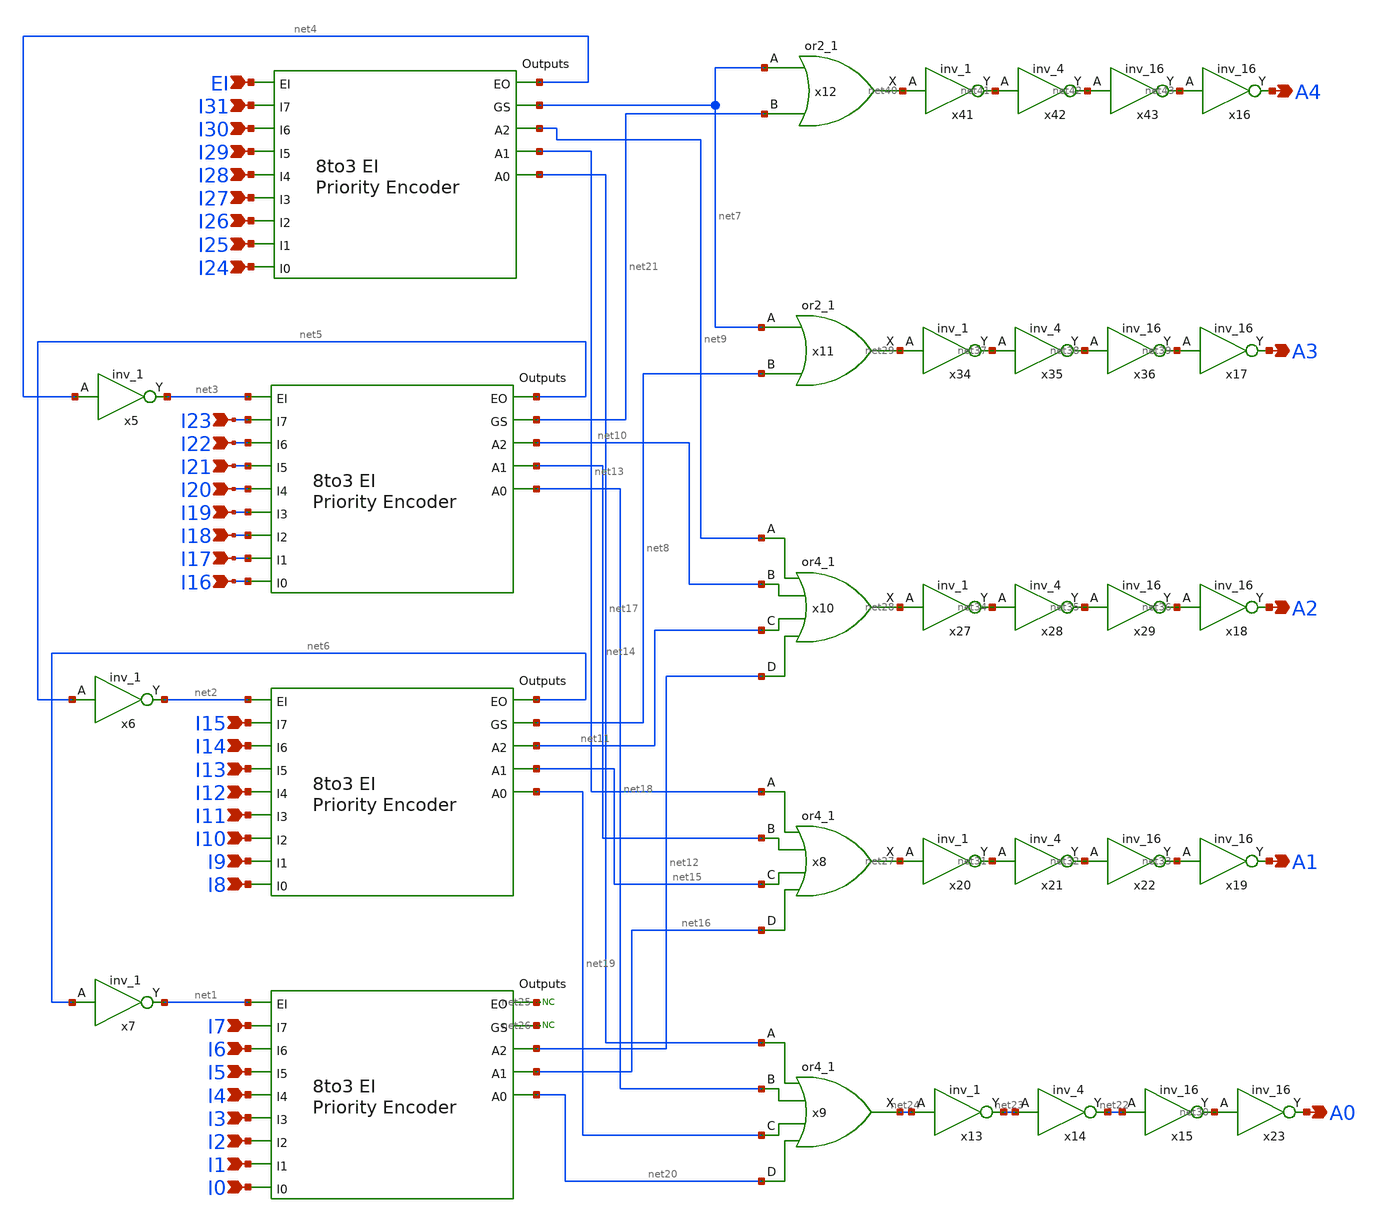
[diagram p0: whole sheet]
** sch_path: PriorityEncoder/32to5_Priority_Encoder_v0p2p2.sch
.lib $::SKYWATER_MODELS/sky130.lib.spice tt
.include $::SKYWATER_STDCELLS/sky130_fd_sc_hd.spice

**.subckt 32to5_Priority_Encoder_v0p2p2 EI I31 I30 I29 I28 I27 I26 I25 I24 I23 I22 I21 I20 I19 I18
*+ I17 I16 I15 I14 I13 I12 I11 I10 I9 I8 I7 I6 I5 I4 I3 I2 I1 I0 A4 A3 A2 A1 A0
*.ipin EI
*.ipin I31
*.ipin I30
*.ipin I29
*.ipin I28
*.ipin I27
*.ipin I26
*.ipin I25
*.ipin I24
*.ipin I23
*.ipin I22
*.ipin I21
*.ipin I20
*.ipin I19
*.ipin I18
*.ipin I17
*.ipin I16
*.ipin I15
*.ipin I14
*.ipin I13
*.ipin I12
*.ipin I11
*.ipin I10
*.ipin I9
*.ipin I8
*.ipin I7
*.ipin I6
*.ipin I5
*.ipin I4
*.ipin I3
*.ipin I2
*.ipin I1
*.ipin I0
*.opin A4
*.opin A3
*.opin A2
*.opin A1
*.opin A0
x1 I25 I29 I27 I24 I26 I30 I31 I28 net4 net7 net9 net13 net17 EI 8to3_Priority_Encoder_v0p2p0
x2 I17 I21 I19 I16 I18 I22 I23 I20 net5 net21 net10 net14 net18 net3 8to3_Priority_Encoder_v0p2p0
x3 I9 I13 I11 I8 I10 I14 I15 I12 net6 net8 net11 net15 net19 net2 8to3_Priority_Encoder_v0p2p0
x4 I1 I5 I3 I0 I2 I6 I7 I4 net25 net26 net12 net16 net20 net1 8to3_Priority_Encoder_v0p2p0
x5 net4 GND GND VDD VDD net3 sky130_fd_sc_hd__inv_1
x9 net17 net18 net19 net20 GND GND VDD VDD net24 sky130_fd_sc_hd__or4_1
x8 net13 net14 net15 net16 GND GND VDD VDD net27 sky130_fd_sc_hd__or4_1
x10 net9 net10 net11 net12 GND GND VDD VDD net28 sky130_fd_sc_hd__or4_1
x11 net7 net8 GND GND VDD VDD net29 sky130_fd_sc_hd__or2_1
x13 net24 GND GND VDD VDD net23 sky130_fd_sc_hd__inv_1
x14 net23 GND GND VDD VDD net22 sky130_fd_sc_hd__inv_4
x15 net22 GND GND VDD VDD net30 sky130_fd_sc_hd__inv_16
x20 net27 GND GND VDD VDD net31 sky130_fd_sc_hd__inv_1
x21 net31 GND GND VDD VDD net32 sky130_fd_sc_hd__inv_4
x22 net32 GND GND VDD VDD net33 sky130_fd_sc_hd__inv_16
x27 net28 GND GND VDD VDD net34 sky130_fd_sc_hd__inv_1
x28 net34 GND GND VDD VDD net35 sky130_fd_sc_hd__inv_4
x29 net35 GND GND VDD VDD net36 sky130_fd_sc_hd__inv_16
x34 net29 GND GND VDD VDD net37 sky130_fd_sc_hd__inv_1
x35 net37 GND GND VDD VDD net38 sky130_fd_sc_hd__inv_4
x36 net38 GND GND VDD VDD net39 sky130_fd_sc_hd__inv_16
x12 net7 net21 GND GND VDD VDD net40 sky130_fd_sc_hd__or2_1
x41 net40 GND GND VDD VDD net41 sky130_fd_sc_hd__inv_1
x42 net41 GND GND VDD VDD net42 sky130_fd_sc_hd__inv_4
x43 net42 GND GND VDD VDD net43 sky130_fd_sc_hd__inv_16
* noconn #net25
* noconn #net26
x16 net43 GND GND VDD VDD A4 sky130_fd_sc_hd__inv_16
x17 net39 GND GND VDD VDD A3 sky130_fd_sc_hd__inv_16
x18 net36 GND GND VDD VDD A2 sky130_fd_sc_hd__inv_16
x19 net33 GND GND VDD VDD A1 sky130_fd_sc_hd__inv_16
x23 net30 GND GND VDD VDD A0 sky130_fd_sc_hd__inv_16
x6 net5 GND GND VDD VDD net2 sky130_fd_sc_hd__inv_1
x7 net6 GND GND VDD VDD net1 sky130_fd_sc_hd__inv_1
**.ends
.end
